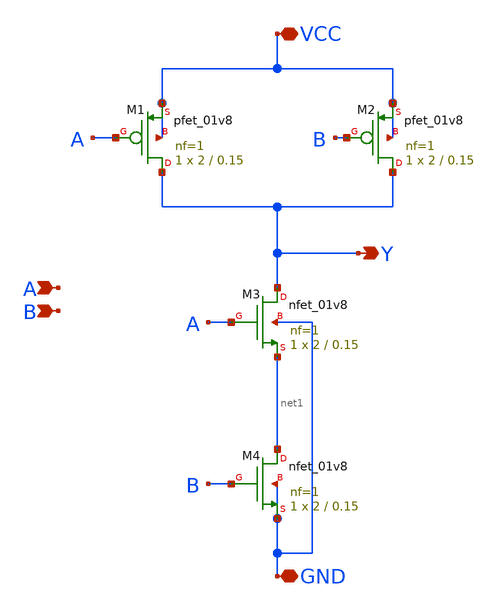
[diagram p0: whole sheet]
** sch_path: blocks/03_StrongARM/xschem/NAND2.sch
**.subckt NAND2 VCC GND A B Y
*.iopin VCC
*.iopin GND
*.ipin A
*.ipin B
*.opin Y
XM1 Y A VCC VCC sky130_fd_pr__pfet_01v8 L=0.15 W=2 nf=1 ad='int((1 + 1)/2) * 2 / 1 * 0.29' as='int((1 + 2)/2) * 2 / 1 * 0.29'
+ pd='2*int((1 + 1)/2) * (2 / 1 + 0.29)' ps='2*int((1 + 2)/2) * (2 / 1 + 0.29)' nrd='0.29 / 2 ' nrs='0.29 / 2 '
+ sa=0 sb=0 sd=0 mult=1 m=1
XM2 Y B VCC VCC sky130_fd_pr__pfet_01v8 L=0.15 W=2 nf=1 ad='int((1 + 1)/2) * 2 / 1 * 0.29' as='int((1 + 2)/2) * 2 / 1 * 0.29'
+ pd='2*int((1 + 1)/2) * (2 / 1 + 0.29)' ps='2*int((1 + 2)/2) * (2 / 1 + 0.29)' nrd='0.29 / 2 ' nrs='0.29 / 2 '
+ sa=0 sb=0 sd=0 mult=1 m=1
XM3 Y A net1 GND sky130_fd_pr__nfet_01v8 L=0.15 W=2 nf=1 ad='int((1 + 1)/2) * 2 / 1 * 0.29' as='int((1 + 2)/2) * 2 / 1 * 0.29'
+ pd='2*int((1 + 1)/2) * (2 / 1 + 0.29)' ps='2*int((1 + 2)/2) * (2 / 1 + 0.29)' nrd='0.29 / 2 ' nrs='0.29 / 2 '
+ sa=0 sb=0 sd=0 mult=1 m=1
XM4 net1 B GND GND sky130_fd_pr__nfet_01v8 L=0.15 W=2 nf=1 ad='int((1 + 1)/2) * 2 / 1 * 0.29' as='int((1 + 2)/2) * 2 / 1 * 0.29'
+ pd='2*int((1 + 1)/2) * (2 / 1 + 0.29)' ps='2*int((1 + 2)/2) * (2 / 1 + 0.29)' nrd='0.29 / 2 ' nrs='0.29 / 2 '
+ sa=0 sb=0 sd=0 mult=1 m=1
**.ends
.end
